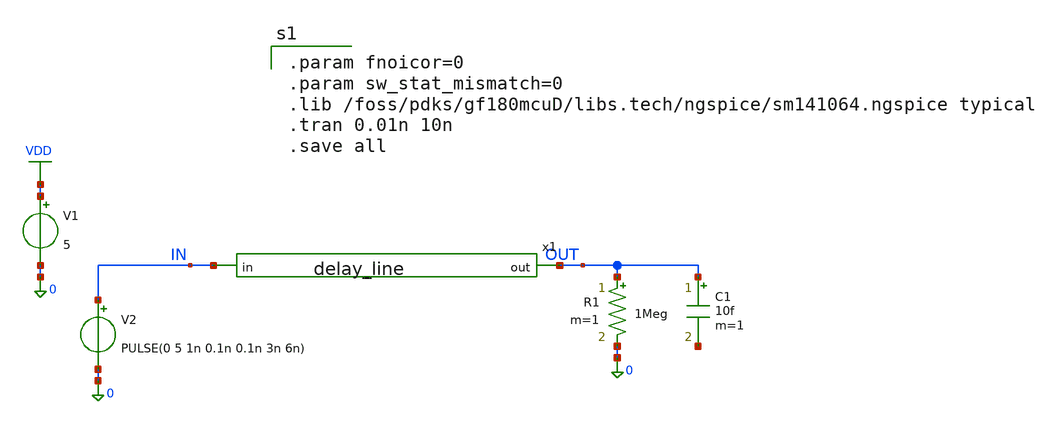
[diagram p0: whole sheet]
** sch_path: xschem/sar_adc/blocks/async_sar/testbench/tb_delay_line.sch
**.subckt tb_delay_line
V1 VDD 0 5
V2 IN 0 PULSE(0 5 1n 0.1n 0.1n 3n 6n)
R1 OUT 0 1Meg m=1
x1 OUT IN delay_line
C1 OUT net1 10f m=1
**** begin user architecture code

.param fnoicor=0
.param sw_stat_mismatch=0
.lib /foss/pdks/gf180mcuD/libs.tech/ngspice/sm141064.ngspice typical
.tran 0.01n 10n
.save all

**** end user architecture code
**.ends
.GLOBAL VDD
.end
